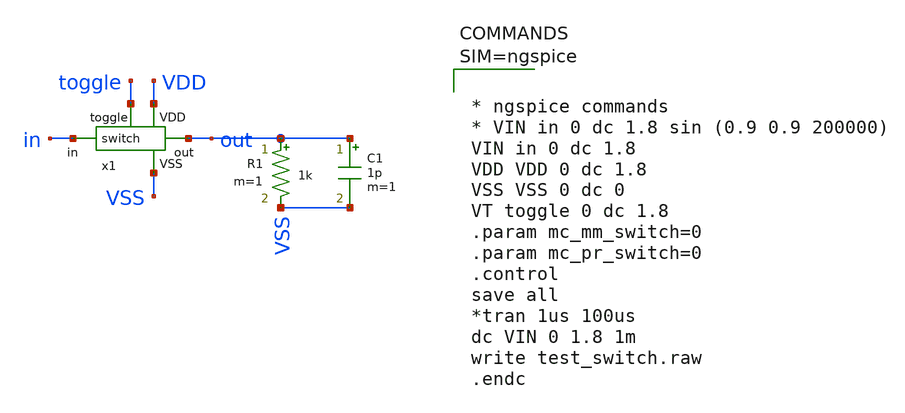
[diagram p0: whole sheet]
** sch_path: xschem/test_switch.sch
**.subckt test_switch
x1 toggle out in VDD VSS switch
R1 out VSS 1k m=1
C1 out VSS 1p m=1
**** begin user architecture code

** opencircuitdesign pdks install
.lib $::SKYWATER_MODELS/sky130.lib.spice tt





* ngspice commands
* VIN in 0 dc 1.8 sin (0.9 0.9 200000)
VIN in 0 dc 1.8
VDD VDD 0 dc 1.8
VSS VSS 0 dc 0
VT toggle 0 dc 1.8
.param mc_mm_switch=0
.param mc_pr_switch=0
.control
save all
*tran 1us 100us
dc VIN 0 1.8 1m
write test_switch.raw
.endc


**** end user architecture code
**.ends

* expanding   symbol:  switch/switch.sym # of pins=5
** sym_path: xschem/switch/switch.sym
** sch_path: xschem/switch/switch.sch
.subckt switch toggle out in VDD VSS
*.ipin toggle
*.ipin in
*.opin out
*.iopin VDD
*.iopin VSS
x1 VDD toggle net1 VSS not
XM26 out net1 in VDD sky130_fd_pr__pfet_01v8_lvt L=3 W=200 nf=5 ad='int((5 + 1)/2) * 200 / 5 * 0.29'
+ as='int((5 + 2)/2) * 200 / 5 * 0.29' pd='2*int((5 + 1)/2) * (200 / 5 + 0.29)' ps='2*int((5 + 2)/2) * (200 / 5 + 0.29)'
+ nrd='0.29 / 200 ' nrs='0.29 / 200 ' sa=0 sb=0 sd=0 mult=1 m=1
XM17 in toggle out VSS sky130_fd_pr__nfet_01v8_lvt L=3 W=200 nf=5 ad='int((5 + 1)/2) * 200 / 5 * 0.29'
+ as='int((5 + 2)/2) * 200 / 5 * 0.29' pd='2*int((5 + 1)/2) * (200 / 5 + 0.29)' ps='2*int((5 + 2)/2) * (200 / 5 + 0.29)'
+ nrd='0.29 / 200 ' nrs='0.29 / 200 ' sa=0 sb=0 sd=0 mult=1 m=1
.ends


* expanding   symbol:  not/not.sym # of pins=4
** sym_path: xschem/not/not.sym
** sch_path: xschem/not/not.sch
.subckt not VDD in out VSS
*.ipin in
*.opin out
*.iopin VDD
*.iopin VSS
XM10 out in VDD VDD sky130_fd_pr__pfet_01v8_lvt L=0.35 W=2 nf=1 ad='int((1 + 1)/2) * 2 / 1 * 0.29' as='int((1 + 2)/2) * 2 / 1 * 0.29'
+ pd='2*int((1 + 1)/2) * (2 / 1 + 0.29)' ps='2*int((1 + 2)/2) * (2 / 1 + 0.29)' nrd='0.29 / 2 ' nrs='0.29 / 2 '
+ sa=0 sb=0 sd=0 mult=1 m=1
XM1 out in VSS VSS sky130_fd_pr__nfet_01v8_lvt L=0.35 W=1 nf=1 ad='int((1 + 1)/2) * 1 / 1 * 0.29' as='int((1 + 2)/2) * 1 / 1 * 0.29'
+ pd='2*int((1 + 1)/2) * (1 / 1 + 0.29)' ps='2*int((1 + 2)/2) * (1 / 1 + 0.29)' nrd='0.29 / 1 ' nrs='0.29 / 1 '
+ sa=0 sb=0 sd=0 mult=1 m=1
.ends

.end
